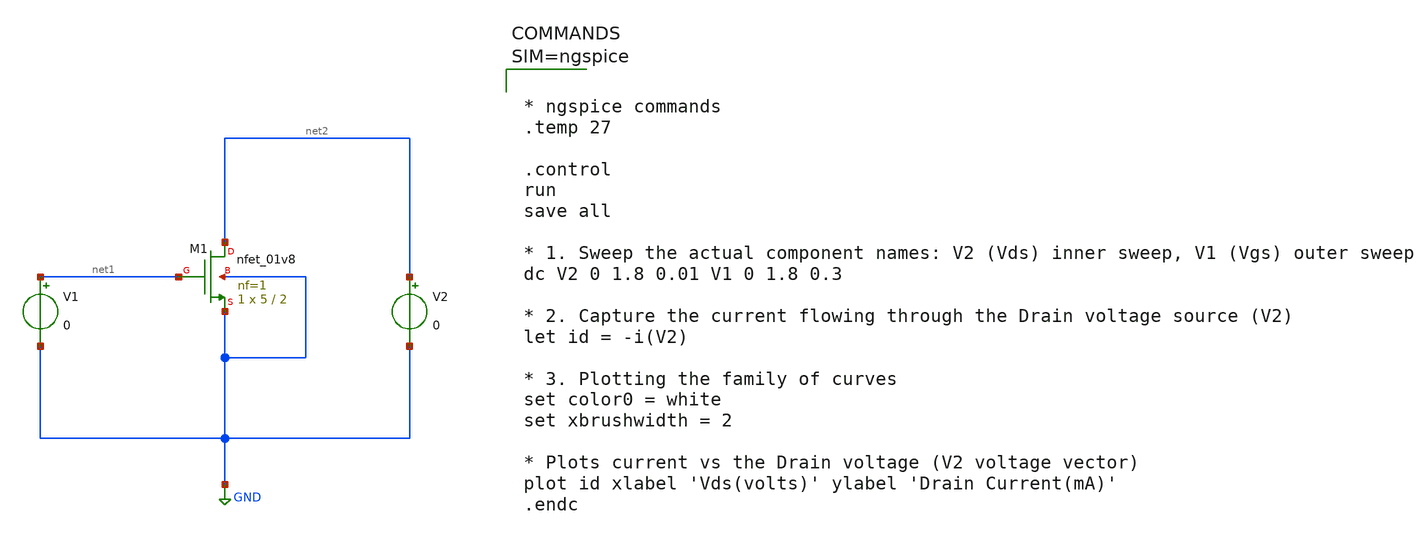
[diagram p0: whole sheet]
** sch_path: testbenches/NMOS_Id_Vds.sch
**.subckt NMOS_Id_Vds
XM1 net2 net1 GND GND sky130_fd_pr__nfet_01v8 L=2 W=5 nf=1 ad='int((1 + 1)/2) * 5 / 1 * 0.29' as='int((1 + 2)/2) * 5 / 1 * 0.29'
+ pd='2*int((1 + 1)/2) * (5 / 1 + 0.29)' ps='2*int((1 + 2)/2) * (5 / 1 + 0.29)' nrd='0.29 / 5 ' nrs='0.29 / 5 '
+ sa=0 sb=0 sd=0 mult=1 m=1
V1 net1 GND 0
V2 net2 GND 0
**** begin user architecture code

** opencircuitdesign pdks install
.lib $::SKYWATER_MODELS/sky130.lib.spice tt




* ngspice commands
.temp 27

.control
run
save all

* 1. Sweep the actual component names: V2 (Vds) inner sweep, V1 (Vgs) outer sweep
dc V2 0 1.8 0.01 V1 0 1.8 0.3

* 2. Capture the current flowing through the Drain voltage source (V2)
let id = -i(V2)

* 3. Plotting the family of curves
set color0 = white
set xbrushwidth = 2

* Plots current vs the Drain voltage (V2 voltage vector)
plot id xlabel 'Vds(volts)' ylabel 'Drain Current(mA)'
.endc



**** end user architecture code
**.ends
.GLOBAL GND
.end
